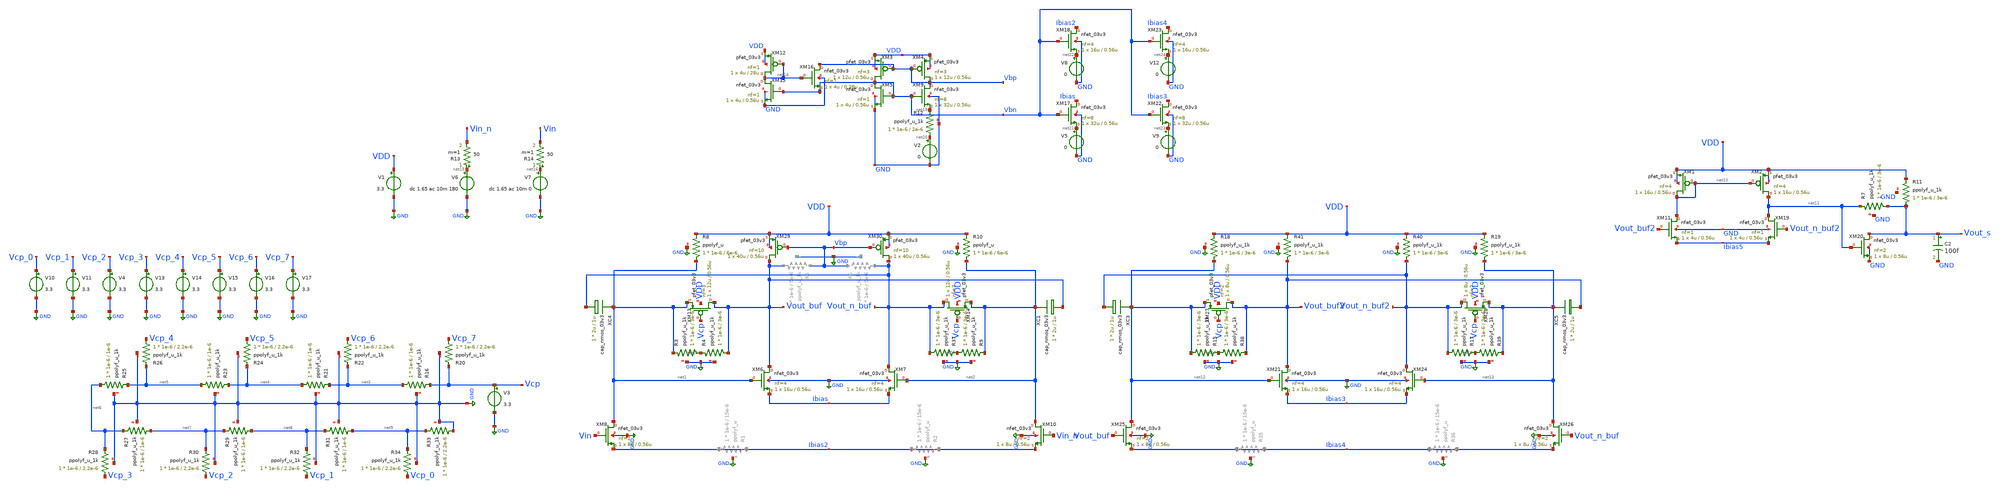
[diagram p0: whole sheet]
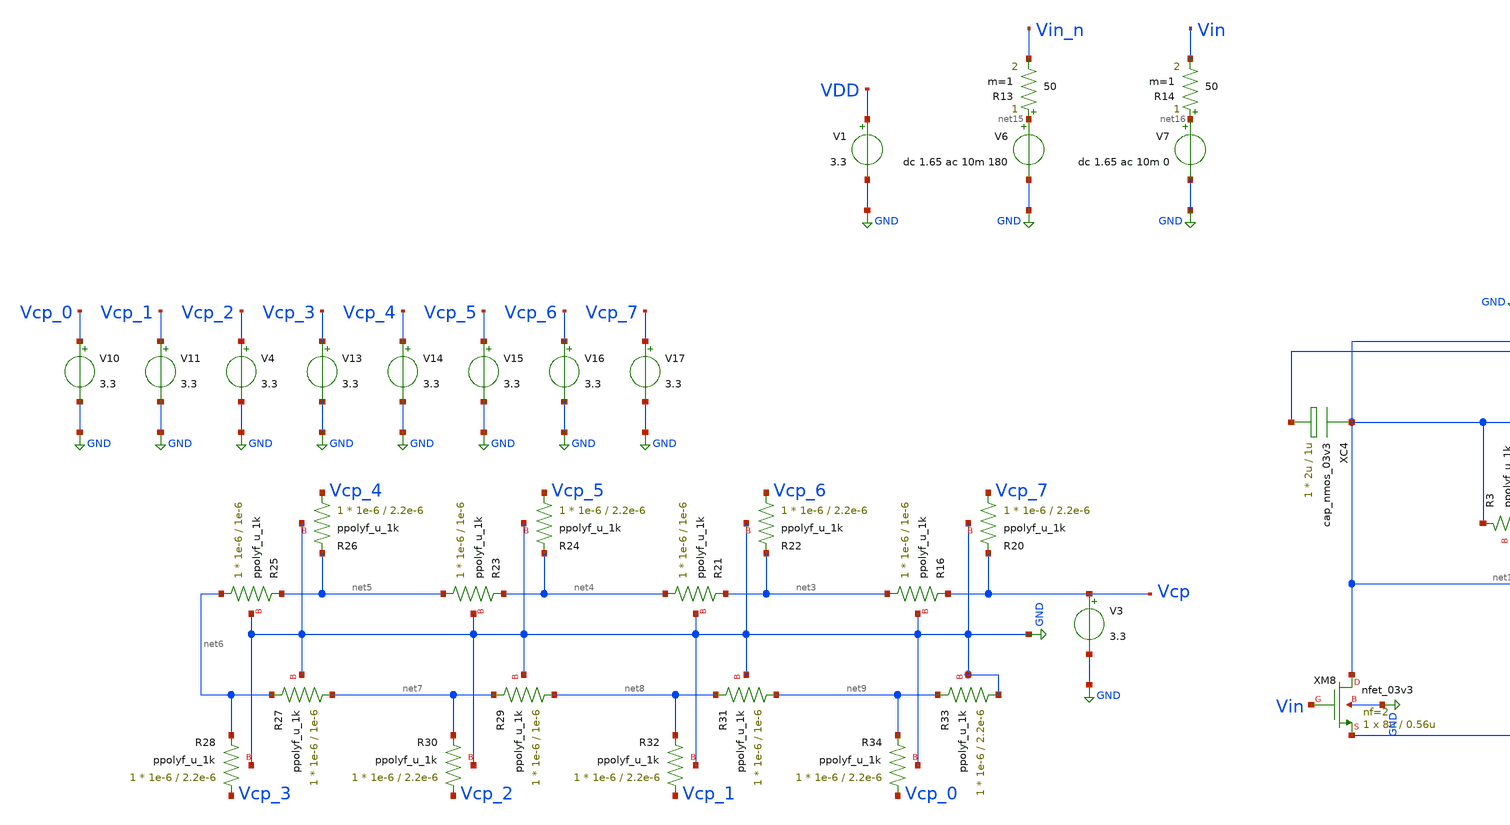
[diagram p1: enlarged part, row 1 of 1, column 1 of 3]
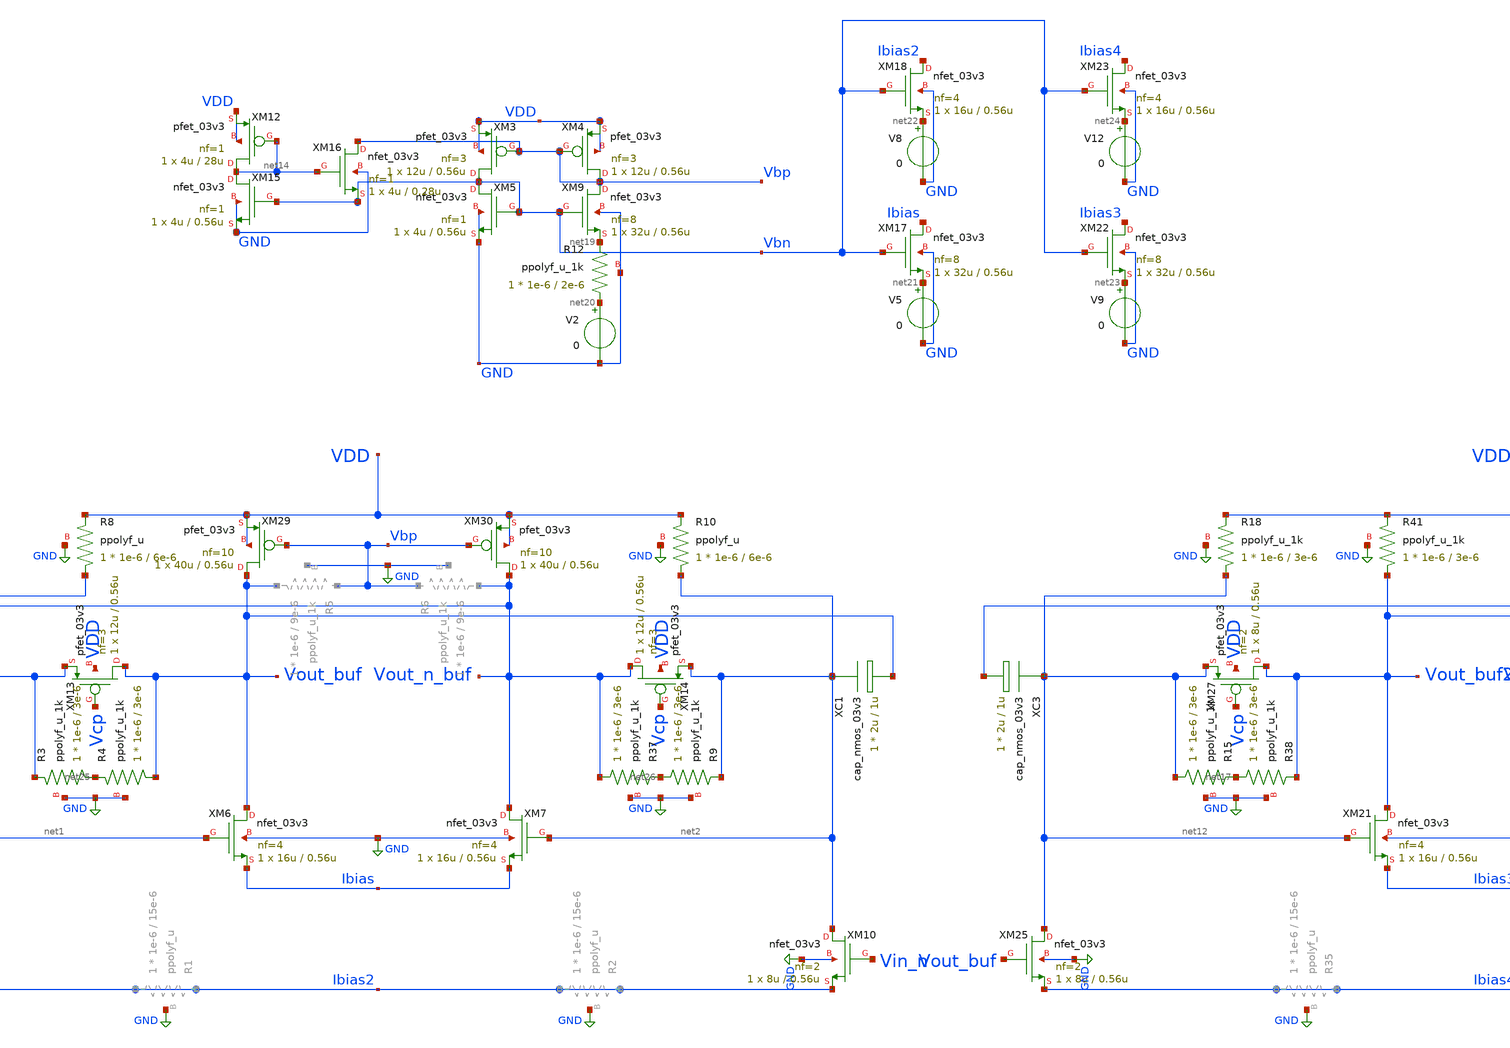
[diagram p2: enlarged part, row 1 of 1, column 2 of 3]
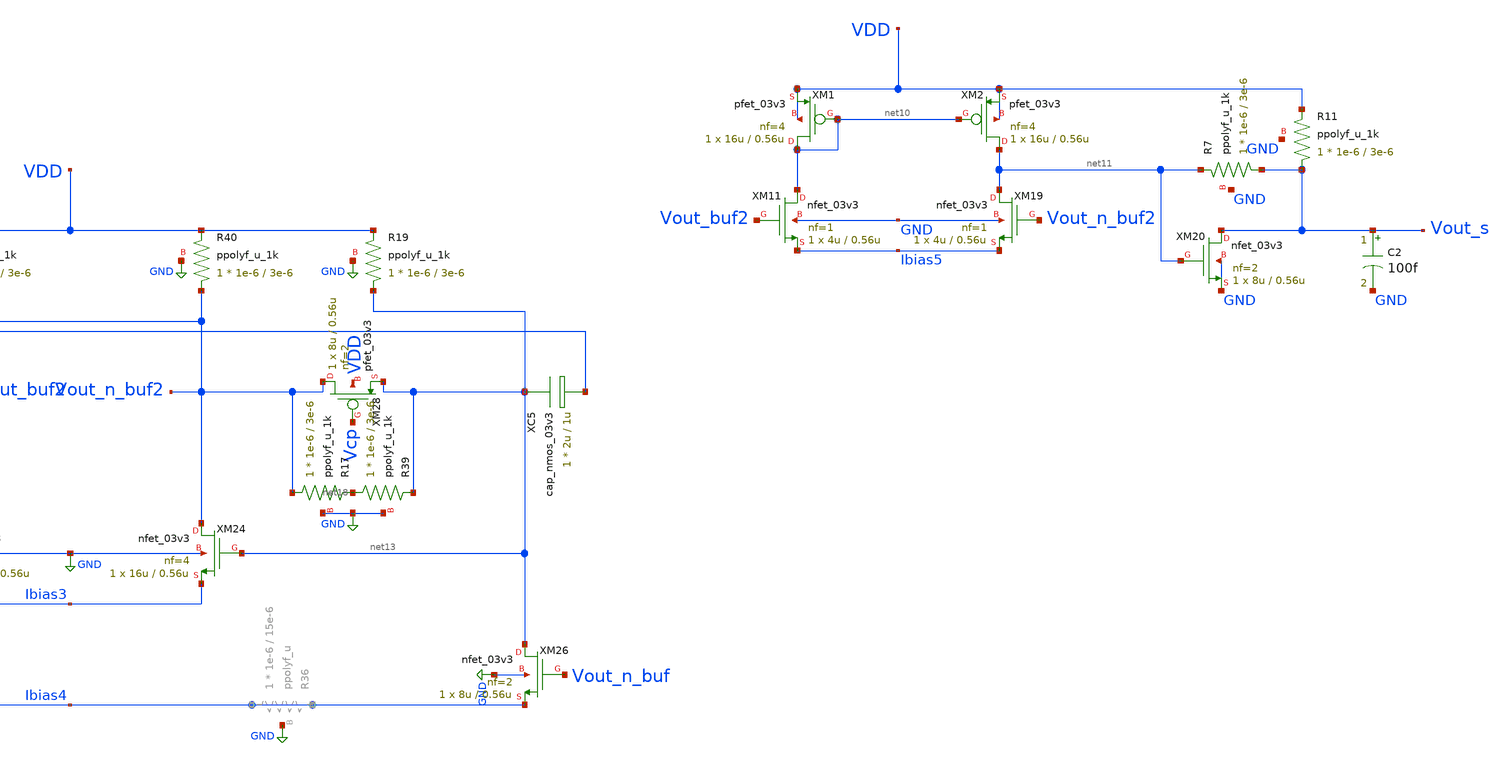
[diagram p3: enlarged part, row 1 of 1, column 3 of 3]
** sch_path: blocks/vga/vga.sch
**.subckt vga
V1 VDD GND 3.3
V6 net15 GND dc 1.65 ac 10m 180
XM6 Vout_buf net1 Ibias GND nfet_03v3 L=0.56u W=16u nf=4 ad='int((nf+1)/2) * W/nf * 0.18u' as='int((nf+2)/2) * W/nf * 0.18u'
+ pd='2*int((nf+1)/2) * (W/nf + 0.18u)' ps='2*int((nf+2)/2) * (W/nf + 0.18u)' nrd='0.18u / W' nrs='0.18u / W'
+ sa=0 sb=0 sd=0 m=1
XM7 Vout_n_buf net2 Ibias GND nfet_03v3 L=0.56u W=16u nf=4 ad='int((nf+1)/2) * W/nf * 0.18u' as='int((nf+2)/2) * W/nf * 0.18u'
+ pd='2*int((nf+1)/2) * (W/nf + 0.18u)' ps='2*int((nf+2)/2) * (W/nf + 0.18u)' nrd='0.18u / W' nrs='0.18u / W'
+ sa=0 sb=0 sd=0 m=1
XM8 net1 Vin Ibias2 GND nfet_03v3 L=0.56u W=8u nf=2 ad='int((nf+1)/2) * W/nf * 0.18u' as='int((nf+2)/2) * W/nf * 0.18u'
+ pd='2*int((nf+1)/2) * (W/nf + 0.18u)' ps='2*int((nf+2)/2) * (W/nf + 0.18u)' nrd='0.18u / W' nrs='0.18u / W'
+ sa=0 sb=0 sd=0 m=1
XM10 net2 Vin_n Ibias2 GND nfet_03v3 L=0.56u W=8u nf=2 ad='int((nf+1)/2) * W/nf * 0.18u' as='int((nf+2)/2) * W/nf * 0.18u'
+ pd='2*int((nf+1)/2) * (W/nf + 0.18u)' ps='2*int((nf+2)/2) * (W/nf + 0.18u)' nrd='0.18u / W' nrs='0.18u / W'
+ sa=0 sb=0 sd=0 m=1
V7 net16 GND dc 1.65 ac 10m 0
R14 net16 Vin 50 m=1
R13 net15 Vin_n 50 m=1
XR16 net3 Vcp GND ppolyf_u_1k r_width=1e-6 r_length=1e-6 m=1
XR20 Vcp_7 Vcp GND ppolyf_u_1k r_width=1e-6 r_length=2.2e-6 m=1
XR21 net4 net3 GND ppolyf_u_1k r_width=1e-6 r_length=1e-6 m=1
XR22 Vcp_6 net3 GND ppolyf_u_1k r_width=1e-6 r_length=2.2e-6 m=1
XR23 net5 net4 GND ppolyf_u_1k r_width=1e-6 r_length=1e-6 m=1
XR24 Vcp_5 net4 GND ppolyf_u_1k r_width=1e-6 r_length=2.2e-6 m=1
XR25 net6 net5 GND ppolyf_u_1k r_width=1e-6 r_length=1e-6 m=1
XR26 Vcp_4 net5 GND ppolyf_u_1k r_width=1e-6 r_length=2.2e-6 m=1
XR27 net7 net6 GND ppolyf_u_1k r_width=1e-6 r_length=1e-6 m=1
XR28 Vcp_3 net6 GND ppolyf_u_1k r_width=1e-6 r_length=2.2e-6 m=1
XR29 net8 net7 GND ppolyf_u_1k r_width=1e-6 r_length=1e-6 m=1
XR30 Vcp_2 net7 GND ppolyf_u_1k r_width=1e-6 r_length=2.2e-6 m=1
XR31 net9 net8 GND ppolyf_u_1k r_width=1e-6 r_length=1e-6 m=1
XR32 Vcp_1 net8 GND ppolyf_u_1k r_width=1e-6 r_length=2.2e-6 m=1
XR33 GND net9 GND ppolyf_u_1k r_width=1e-6 r_length=2.2e-6 m=1
XR34 Vcp_0 net9 GND ppolyf_u_1k r_width=1e-6 r_length=2.2e-6 m=1
V10 Vcp_0 GND 3.3
V11 Vcp_1 GND 3.3
V4 Vcp_2 GND 3.3
V13 Vcp_3 GND 3.3
V14 Vcp_4 GND 3.3
V15 Vcp_5 GND 3.3
V16 Vcp_6 GND 3.3
V17 Vcp_7 GND 3.3
V3 Vcp GND 3.3
XM13 Vout_buf Vcp net1 VDD pfet_03v3 L=0.56u W=12u nf=3 ad='int((nf+1)/2) * W/nf * 0.18u' as='int((nf+2)/2) * W/nf * 0.18u'
+ pd='2*int((nf+1)/2) * (W/nf + 0.18u)' ps='2*int((nf+2)/2) * (W/nf + 0.18u)' nrd='0.18u / W' nrs='0.18u / W'
+ sa=0 sb=0 sd=0 m=1
XM14 Vout_n_buf Vcp net2 VDD pfet_03v3 L=0.56u W=12u nf=3 ad='int((nf+1)/2) * W/nf * 0.18u' as='int((nf+2)/2) * W/nf * 0.18u'
+ pd='2*int((nf+1)/2) * (W/nf + 0.18u)' ps='2*int((nf+2)/2) * (W/nf + 0.18u)' nrd='0.18u / W' nrs='0.18u / W'
+ sa=0 sb=0 sd=0 m=1
XR8 net1 VDD GND ppolyf_u r_width=1e-6 r_length=6e-6 m=1
XR10 net2 VDD GND ppolyf_u r_width=1e-6 r_length=6e-6 m=1
XC4 net1 Vout_n_buf cap_nmos_03v3 c_width=2u c_length=1u m=1
XC1 net2 Vout_buf cap_nmos_03v3 c_width=2u c_length=1u m=1
XM11 net10 Vout_buf2 Ibias5 GND nfet_03v3 L=0.56u W=4u nf=1 ad='int((nf+1)/2) * W/nf * 0.18u' as='int((nf+2)/2) * W/nf * 0.18u'
+ pd='2*int((nf+1)/2) * (W/nf + 0.18u)' ps='2*int((nf+2)/2) * (W/nf + 0.18u)' nrd='0.18u / W' nrs='0.18u / W'
+ sa=0 sb=0 sd=0 m=1
XM19 net11 Vout_n_buf2 Ibias5 GND nfet_03v3 L=0.56u W=4u nf=1 ad='int((nf+1)/2) * W/nf * 0.18u' as='int((nf+2)/2) * W/nf * 0.18u'
+ pd='2*int((nf+1)/2) * (W/nf + 0.18u)' ps='2*int((nf+2)/2) * (W/nf + 0.18u)' nrd='0.18u / W' nrs='0.18u / W'
+ sa=0 sb=0 sd=0 m=1
XR7 Vout_s net11 GND ppolyf_u_1k r_width=1e-6 r_length=3e-6 m=1
XM20 Vout_s net11 GND GND nfet_03v3 L=0.56u W=8u nf=2 ad='int((nf+1)/2) * W/nf * 0.18u' as='int((nf+2)/2) * W/nf * 0.18u'
+ pd='2*int((nf+1)/2) * (W/nf + 0.18u)' ps='2*int((nf+2)/2) * (W/nf + 0.18u)' nrd='0.18u / W' nrs='0.18u / W'
+ sa=0 sb=0 sd=0 m=1
C2 Vout_s GND 100f m=1
XR11 Vout_s VDD GND ppolyf_u_1k r_width=1e-6 r_length=3e-6 m=1
XM1 net10 net10 VDD VDD pfet_03v3 L=0.56u W=16u nf=4 ad='int((nf+1)/2) * W/nf * 0.18u' as='int((nf+2)/2) * W/nf * 0.18u'
+ pd='2*int((nf+1)/2) * (W/nf + 0.18u)' ps='2*int((nf+2)/2) * (W/nf + 0.18u)' nrd='0.18u / W' nrs='0.18u / W'
+ sa=0 sb=0 sd=0 m=1
XM2 net11 net10 VDD VDD pfet_03v3 L=0.56u W=16u nf=4 ad='int((nf+1)/2) * W/nf * 0.18u' as='int((nf+2)/2) * W/nf * 0.18u'
+ pd='2*int((nf+1)/2) * (W/nf + 0.18u)' ps='2*int((nf+2)/2) * (W/nf + 0.18u)' nrd='0.18u / W' nrs='0.18u / W'
+ sa=0 sb=0 sd=0 m=1
XM21 Vout_buf2 net12 Ibias3 GND nfet_03v3 L=0.56u W=16u nf=4 ad='int((nf+1)/2) * W/nf * 0.18u' as='int((nf+2)/2) * W/nf * 0.18u'
+ pd='2*int((nf+1)/2) * (W/nf + 0.18u)' ps='2*int((nf+2)/2) * (W/nf + 0.18u)' nrd='0.18u / W' nrs='0.18u / W'
+ sa=0 sb=0 sd=0 m=1
XM24 Vout_n_buf2 net13 Ibias3 GND nfet_03v3 L=0.56u W=16u nf=4 ad='int((nf+1)/2) * W/nf * 0.18u' as='int((nf+2)/2) * W/nf * 0.18u'
+ pd='2*int((nf+1)/2) * (W/nf + 0.18u)' ps='2*int((nf+2)/2) * (W/nf + 0.18u)' nrd='0.18u / W' nrs='0.18u / W'
+ sa=0 sb=0 sd=0 m=1
XM25 net12 Vout_buf Ibias4 GND nfet_03v3 L=0.56u W=8u nf=2 ad='int((nf+1)/2) * W/nf * 0.18u' as='int((nf+2)/2) * W/nf * 0.18u'
+ pd='2*int((nf+1)/2) * (W/nf + 0.18u)' ps='2*int((nf+2)/2) * (W/nf + 0.18u)' nrd='0.18u / W' nrs='0.18u / W'
+ sa=0 sb=0 sd=0 m=1
XM26 net13 Vout_n_buf Ibias4 GND nfet_03v3 L=0.56u W=8u nf=2 ad='int((nf+1)/2) * W/nf * 0.18u' as='int((nf+2)/2) * W/nf * 0.18u'
+ pd='2*int((nf+1)/2) * (W/nf + 0.18u)' ps='2*int((nf+2)/2) * (W/nf + 0.18u)' nrd='0.18u / W' nrs='0.18u / W'
+ sa=0 sb=0 sd=0 m=1
XM27 Vout_buf2 Vcp net12 VDD pfet_03v3 L=0.56u W=8u nf=2 ad='int((nf+1)/2) * W/nf * 0.18u' as='int((nf+2)/2) * W/nf * 0.18u'
+ pd='2*int((nf+1)/2) * (W/nf + 0.18u)' ps='2*int((nf+2)/2) * (W/nf + 0.18u)' nrd='0.18u / W' nrs='0.18u / W'
+ sa=0 sb=0 sd=0 m=1
XR15 net12 net17 GND ppolyf_u_1k r_width=1e-6 r_length=3e-6 m=1
XM28 Vout_n_buf2 Vcp net13 VDD pfet_03v3 L=0.56u W=8u nf=2 ad='int((nf+1)/2) * W/nf * 0.18u' as='int((nf+2)/2) * W/nf * 0.18u'
+ pd='2*int((nf+1)/2) * (W/nf + 0.18u)' ps='2*int((nf+2)/2) * (W/nf + 0.18u)' nrd='0.18u / W' nrs='0.18u / W'
+ sa=0 sb=0 sd=0 m=1
XR17 Vout_n_buf2 net18 GND ppolyf_u_1k r_width=1e-6 r_length=3e-6 m=1
XR18 net12 VDD GND ppolyf_u_1k r_width=1e-6 r_length=3e-6 m=1
XR19 net13 VDD GND ppolyf_u_1k r_width=1e-6 r_length=3e-6 m=1
XR38 net17 Vout_buf2 GND ppolyf_u_1k r_width=1e-6 r_length=3e-6 m=1
XR39 net18 net13 GND ppolyf_u_1k r_width=1e-6 r_length=3e-6 m=1
XR40 Vout_n_buf2 VDD GND ppolyf_u_1k r_width=1e-6 r_length=3e-6 m=1
XR41 Vout_buf2 VDD GND ppolyf_u_1k r_width=1e-6 r_length=3e-6 m=1
XC3 net12 Vout_n_buf2 cap_nmos_03v3 c_width=2u c_length=1u m=1
XC5 net13 Vout_buf2 cap_nmos_03v3 c_width=2u c_length=1u m=1
XM3 Vbn Vbp VDD VDD pfet_03v3 L=0.56u W=12u nf=3 ad='int((nf+1)/2) * W/nf * 0.18u' as='int((nf+2)/2) * W/nf * 0.18u'
+ pd='2*int((nf+1)/2) * (W/nf + 0.18u)' ps='2*int((nf+2)/2) * (W/nf + 0.18u)' nrd='0.18u / W' nrs='0.18u / W'
+ sa=0 sb=0 sd=0 m=1
XM4 Vbp Vbp VDD VDD pfet_03v3 L=0.56u W=12u nf=3 ad='int((nf+1)/2) * W/nf * 0.18u' as='int((nf+2)/2) * W/nf * 0.18u'
+ pd='2*int((nf+1)/2) * (W/nf + 0.18u)' ps='2*int((nf+2)/2) * (W/nf + 0.18u)' nrd='0.18u / W' nrs='0.18u / W'
+ sa=0 sb=0 sd=0 m=1
XM5 Vbn Vbn GND GND nfet_03v3 L=0.56u W=4u nf=1 ad='int((nf+1)/2) * W/nf * 0.18u' as='int((nf+2)/2) * W/nf * 0.18u'
+ pd='2*int((nf+1)/2) * (W/nf + 0.18u)' ps='2*int((nf+2)/2) * (W/nf + 0.18u)' nrd='0.18u / W' nrs='0.18u / W'
+ sa=0 sb=0 sd=0 m=1
XM9 Vbp Vbn net19 GND nfet_03v3 L=0.56u W=32u nf=8 ad='int((nf+1)/2) * W/nf * 0.18u' as='int((nf+2)/2) * W/nf * 0.18u'
+ pd='2*int((nf+1)/2) * (W/nf + 0.18u)' ps='2*int((nf+2)/2) * (W/nf + 0.18u)' nrd='0.18u / W' nrs='0.18u / W'
+ sa=0 sb=0 sd=0 m=1
XM12 net14 net14 VDD VDD pfet_03v3 L=28u W=4u nf=1 ad='int((nf+1)/2) * W/nf * 0.18u' as='int((nf+2)/2) * W/nf * 0.18u'
+ pd='2*int((nf+1)/2) * (W/nf + 0.18u)' ps='2*int((nf+2)/2) * (W/nf + 0.18u)' nrd='0.18u / W' nrs='0.18u / W'
+ sa=0 sb=0 sd=0 m=1
XM15 net14 Vbn GND GND nfet_03v3 L=0.56u W=4u nf=1 ad='int((nf+1)/2) * W/nf * 0.18u' as='int((nf+2)/2) * W/nf * 0.18u'
+ pd='2*int((nf+1)/2) * (W/nf + 0.18u)' ps='2*int((nf+2)/2) * (W/nf + 0.18u)' nrd='0.18u / W' nrs='0.18u / W'
+ sa=0 sb=0 sd=0 m=1
XM16 Vbp net14 Vbn GND nfet_03v3 L=0.28u W=4u nf=1 ad='int((nf+1)/2) * W/nf * 0.18u' as='int((nf+2)/2) * W/nf * 0.18u'
+ pd='2*int((nf+1)/2) * (W/nf + 0.18u)' ps='2*int((nf+2)/2) * (W/nf + 0.18u)' nrd='0.18u / W' nrs='0.18u / W'
+ sa=0 sb=0 sd=0 m=1
XR12 net20 net19 GND ppolyf_u_1k r_width=1e-6 r_length=2e-6 m=1
V2 net20 GND 0
XM17 Ibias Vbn net21 GND nfet_03v3 L=0.56u W=32u nf=8 ad='int((nf+1)/2) * W/nf * 0.18u' as='int((nf+2)/2) * W/nf * 0.18u'
+ pd='2*int((nf+1)/2) * (W/nf + 0.18u)' ps='2*int((nf+2)/2) * (W/nf + 0.18u)' nrd='0.18u / W' nrs='0.18u / W'
+ sa=0 sb=0 sd=0 m=1
V5 net21 GND 0
XM18 Ibias2 Vbn net22 GND nfet_03v3 L=0.56u W=16u nf=4 ad='int((nf+1)/2) * W/nf * 0.18u' as='int((nf+2)/2) * W/nf * 0.18u'
+ pd='2*int((nf+1)/2) * (W/nf + 0.18u)' ps='2*int((nf+2)/2) * (W/nf + 0.18u)' nrd='0.18u / W' nrs='0.18u / W'
+ sa=0 sb=0 sd=0 m=1
V8 net22 GND 0
XM22 Ibias3 Vbn net23 GND nfet_03v3 L=0.56u W=32u nf=8 ad='int((nf+1)/2) * W/nf * 0.18u' as='int((nf+2)/2) * W/nf * 0.18u'
+ pd='2*int((nf+1)/2) * (W/nf + 0.18u)' ps='2*int((nf+2)/2) * (W/nf + 0.18u)' nrd='0.18u / W' nrs='0.18u / W'
+ sa=0 sb=0 sd=0 m=1
V9 net23 GND 0
XM23 Ibias4 Vbn net24 GND nfet_03v3 L=0.56u W=16u nf=4 ad='int((nf+1)/2) * W/nf * 0.18u' as='int((nf+2)/2) * W/nf * 0.18u'
+ pd='2*int((nf+1)/2) * (W/nf + 0.18u)' ps='2*int((nf+2)/2) * (W/nf + 0.18u)' nrd='0.18u / W' nrs='0.18u / W'
+ sa=0 sb=0 sd=0 m=1
V12 net24 GND 0
XM29 Vout_buf Vbp VDD VDD pfet_03v3 L=0.56u W=40u nf=10 ad='int((nf+1)/2) * W/nf * 0.18u' as='int((nf+2)/2) * W/nf * 0.18u'
+ pd='2*int((nf+1)/2) * (W/nf + 0.18u)' ps='2*int((nf+2)/2) * (W/nf + 0.18u)' nrd='0.18u / W' nrs='0.18u / W'
+ sa=0 sb=0 sd=0 m=1
XM30 Vout_n_buf Vbp VDD VDD pfet_03v3 L=0.56u W=40u nf=10 ad='int((nf+1)/2) * W/nf * 0.18u' as='int((nf+2)/2) * W/nf * 0.18u'
+ pd='2*int((nf+1)/2) * (W/nf + 0.18u)' ps='2*int((nf+2)/2) * (W/nf + 0.18u)' nrd='0.18u / W' nrs='0.18u / W'
+ sa=0 sb=0 sd=0 m=1
XR3 net25 net1 GND ppolyf_u_1k r_width=1e-6 r_length=3e-6 m=1
XR4 Vout_buf net25 GND ppolyf_u_1k r_width=1e-6 r_length=3e-6 m=1
XR9 net26 net2 GND ppolyf_u_1k r_width=1e-6 r_length=3e-6 m=1
XR37 Vout_n_buf net26 GND ppolyf_u_1k r_width=1e-6 r_length=3e-6 m=1
**** begin user architecture code


.include /foss/pdks/gf180mcuD/libs.tech/ngspice/design.ngspice
.lib /foss/pdks/gf180mcuD/libs.tech/ngspice/sm141064.ngspice typical
.lib /foss/pdks/gf180mcuD/libs.tech/ngspice/sm141064.ngspice bjt_typical
.lib /foss/pdks/gf180mcuD/libs.tech/ngspice/sm141064.ngspice diode_typical
.lib /foss/pdks/gf180mcuD/libs.tech/ngspice/sm141064.ngspice res_typical
.lib /foss/pdks/gf180mcuD/libs.tech/ngspice/sm141064.ngspice mimcap_typical
.lib /foss/pdks/gf180mcuD/libs.tech/ngspice/sm141064.ngspice moscap_typical
.option method=gear

.control
set temp = 85
  * 1. Setup the sweep parameters
  let v_start = 0
  let v_stop = 3.3
  let v_points = 66
  let v_delta = (v_stop - v_start) / v_points

  * 2. Initialize vectors to store results
  let gain_db_20 = unitvec(v_points + 1)
  let gain_db_1200 = unitvec(v_points + 1)
  let vcp_axis = unitvec(v_points + 1)

  let i = 0
  while i <= v_points
    let v_current = v_start + (i * v_delta)
    alter v3 = v_current   ; Adjust the Vcp source DC value

    * 3. Run AC analysis ONLY at 600MHz to maximize speed
    ac lin 3 0.02G 1.2G

    * 4. Calculate Differential Gain in dB
    * Formula: 20 * log10(|Vout_diff| / |Vin_diff|)
    let vout_mag = mag(v(vout_buf) - v(vout_n_buf))
    *let vout_mag = mag(v(vout_s))
    let vin_mag = mag(v(vin) - v(vin_n))
    let g_val = 20 * log10(vout_mag / vin_mag)

    * 5. Save results to vectors
    let gain_db_20[i] = g_val[1]
    let gain_db_1200[i] = g_val[2]
    let vcp_axis[i] = v_current
    let i = i + 1
    *print mag(v(vout) - v(vout_n))
    *print i(v1)
  end

  * 6. Plot the Gain vs Control Voltage
  plot gain_db_20 gain_db_1200 vs vcp_axis title 'VGA Gain at 20MHz, 1.2GHz vs Vcp, 100fF load' xlabel
+ 'Vcp (V)' ylabel 'Gain (dB)'
.endc


**** end user architecture code
**.ends
.GLOBAL GND
.end
